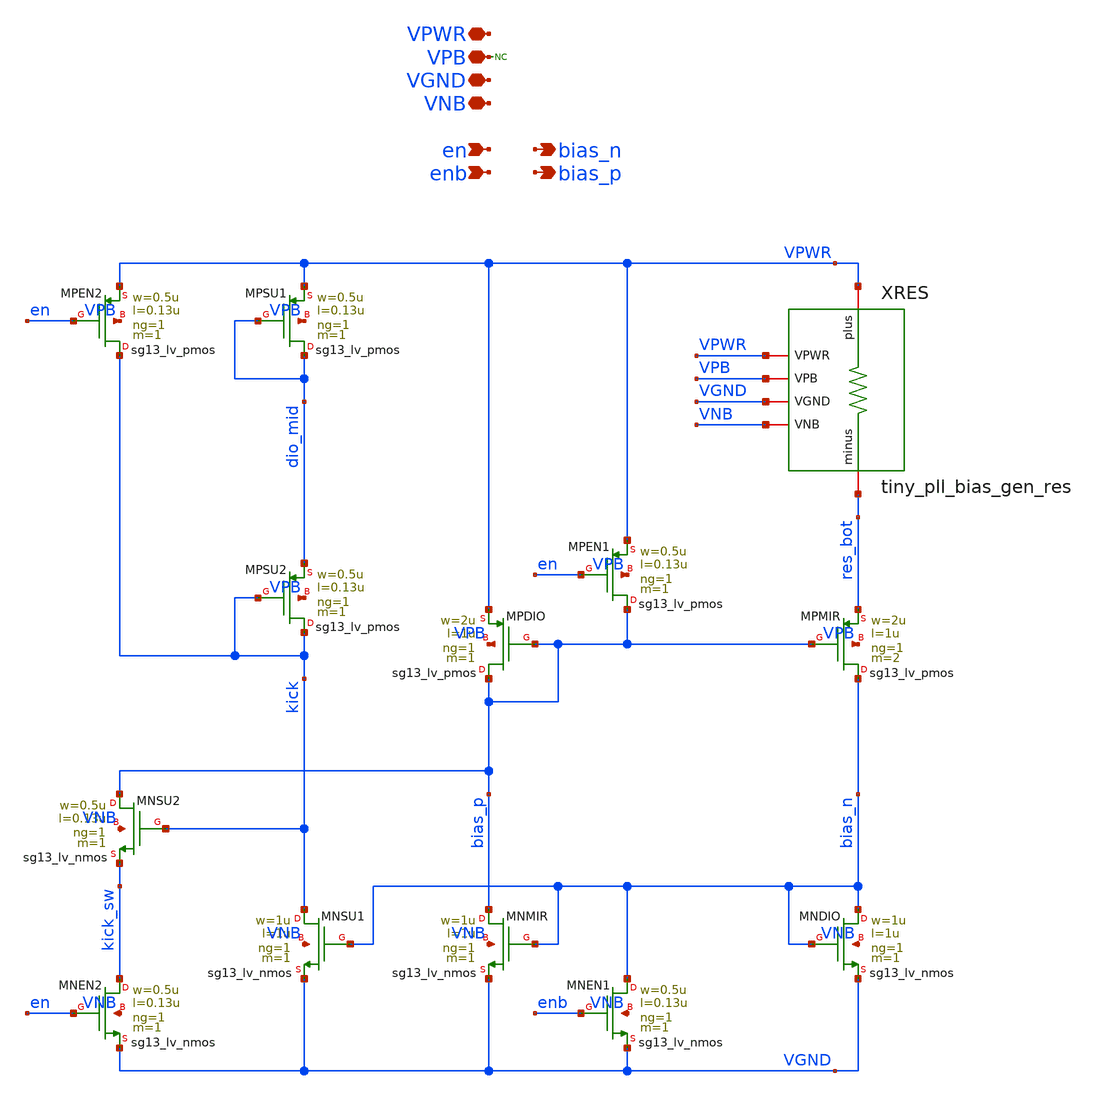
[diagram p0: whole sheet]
** sch_path: xschem/tiny_pll_bias_gen.sch
**.subckt tiny_pll_bias_gen VNB VGND VPB VPWR bias_n enb en bias_p
*.iopin VNB
*.iopin VGND
*.iopin VPB
*.iopin VPWR
*.opin bias_n
*.ipin enb
*.ipin en
*.opin bias_p
XMNMIR bias_p bias_n VGND VNB sg13_lv_nmos w=1u l=1u ng=1 m=1 mm_ok=1
XMNDIO bias_n bias_n VGND VNB sg13_lv_nmos w=1u l=1u ng=1 m=1 mm_ok=1
XMPDIO bias_p bias_p VPWR VPB sg13_lv_pmos w=2u l=1u ng=1 m=1 mm_ok=1
XMPMIR bias_n bias_p res_bot VPB sg13_lv_pmos w=2u l=1u ng=1 m=2 mm_ok=1
* noconn VPB
XMNEN1 bias_n enb VGND VNB sg13_lv_nmos w=0.5u l=0.13u ng=1 m=1 mm_ok=1
XMPEN1 bias_p en VPWR VPB sg13_lv_pmos w=0.5u l=0.13u ng=1 m=1 mm_ok=1
XRES VGND VNB VPWR VPB VPWR res_bot tiny_pll_bias_gen_res
XMNSU1 kick bias_n VGND VNB sg13_lv_nmos w=1u l=1u ng=1 m=1 mm_ok=1
XMNSU2 bias_p kick kick_sw VNB sg13_lv_nmos w=0.5u l=0.13u ng=1 m=1 mm_ok=1
XMNEN2 kick_sw en VGND VNB sg13_lv_nmos w=0.5u l=0.13u ng=1 m=1 mm_ok=1
XMPEN2 kick en VPWR VPB sg13_lv_pmos w=0.5u l=0.13u ng=1 m=1 mm_ok=1
XMPSU2 kick kick dio_mid VPB sg13_lv_pmos w=0.5u l=0.13u ng=1 m=1 mm_ok=1
XMPSU1 dio_mid dio_mid VPWR VPB sg13_lv_pmos w=0.5u l=0.13u ng=1 m=1 mm_ok=1
**.ends

* expanding   symbol:  tiny_pll_bias_gen_res.sym # of pins=6
** sym_path: tiny_pll_bias_gen_res.sym
** sch_path: tiny_pll_bias_gen_res.sch
.subckt tiny_pll_bias_gen_res VGND VNB VPWR VPB plus minus
*.iopin minus
*.iopin plus
*.iopin VNB
*.iopin VGND
*.iopin VPB
*.iopin VPWR
XR2 plus mid1 sub! rhigh w=1.000000e-06 l=2.428235e-06 m=1 b=0 mm_ok=1
XR1 mid1 mid0 sub! rhigh w=1.000000e-06 l=2.428235e-06 m=1 b=0 mm_ok=1
XR0 mid0 minus sub! rhigh w=1.000000e-06 l=2.428235e-06 m=1 b=0 mm_ok=1
* noconn VPB
* noconn VPWR
* noconn VGND
.ends

.end
